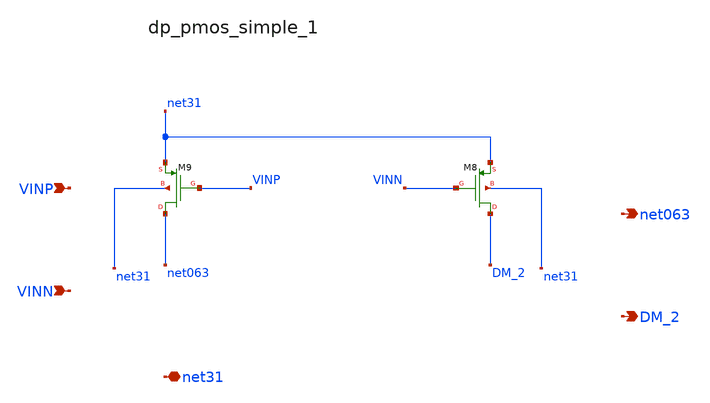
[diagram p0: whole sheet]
** sch_path: analog-db/raw/amp_008_leung_nmcf/hier/blocks/dp_pmos_simple_1.sch
**.subckt dp_pmos_simple_1 VINP VINN net31 net063 DM_2
*.ipin VINP
*.ipin VINN
*.iopin net31
*.opin net063
*.opin DM_2
XM8 DM_2 VINN net31 net31 sg13_lv_pmos w=x_dut_xm8_w l=x_dut_xm8_l ng=1 m=x_dut_xm8_m
XM9 net063 VINP net31 net31 sg13_lv_pmos w=x_dut_xm9_w l=x_dut_xm9_l ng=1 m=x_dut_xm9_m
**.ends
.end
